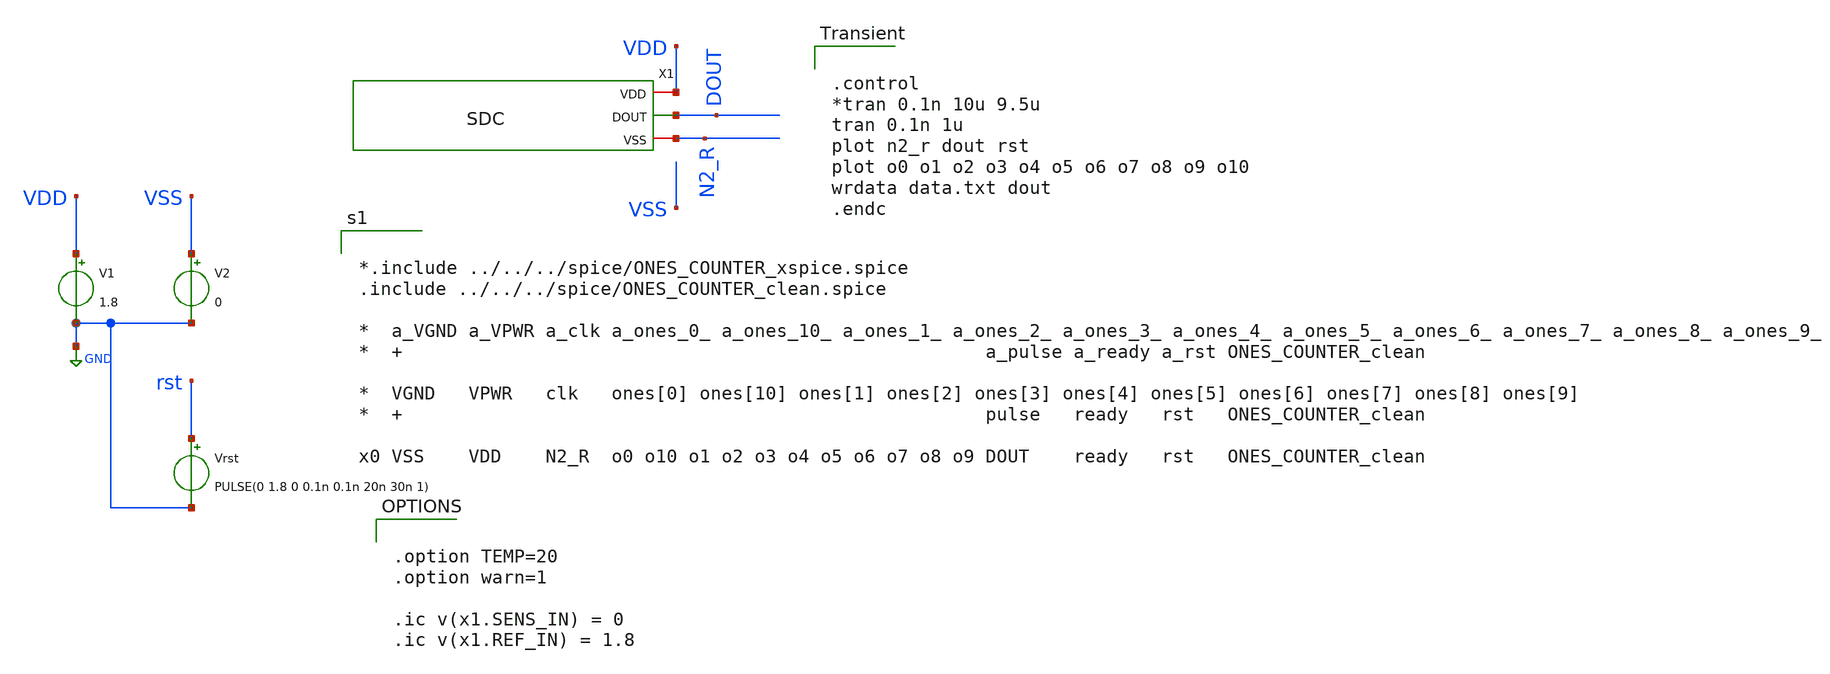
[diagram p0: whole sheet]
** sch_path: modules/ONES_COUNTER/test/transient.sch
**.subckt transient
V1 VDD GND 1.8
V2 VSS GND 0
X1 VDD DOUT N2_R SDC
Vrst rst GND PULSE(0 1.8 0 0.1n 0.1n 20n 30n 1)
**** begin user architecture code


.control
*tran 0.1n 10u 9.5u
tran 0.1n 1u
plot n2_r dout rst
plot o0 o1 o2 o3 o4 o5 o6 o7 o8 o9 o10
wrdata data.txt dout
.endc



.option TEMP=20
.option warn=1

.ic v(x1.SENS_IN) = 0
.ic v(x1.REF_IN) = 1.8



.lib $env(PDK_ROOT)/$env(PDK)/libs.tech/ngspice/sky130.lib.spice tt

.include $env(PDK_ROOT)/$env(PDK)/libs.ref/sky130_fd_sc_hd/spice/sky130_fd_sc_hd.spice



*.include ../../../spice/ONES_COUNTER_xspice.spice
.include ../../../spice/ONES_COUNTER_clean.spice

*  a_VGND a_VPWR a_clk a_ones_0_ a_ones_10_ a_ones_1_ a_ones_2_ a_ones_3_ a_ones_4_ a_ones_5_
*+ a_ones_6_ a_ones_7_ a_ones_8_ a_ones_9_
*  +                                                     a_pulse a_ready a_rst ONES_COUNTER_clean

*  VGND   VPWR   clk   ones[0] ones[10] ones[1] ones[2] ones[3] ones[4] ones[5] ones[6] ones[7]
*+ ones[8] ones[9]
*  +                                                     pulse   ready   rst   ONES_COUNTER_clean

x0 VSS    VDD    N2_R  o0 o10 o1 o2 o3 o4 o5 o6 o7 o8 o9 DOUT    ready   rst   ONES_COUNTER_clean


**** end user architecture code
**.ends
.GLOBAL GND
.end
